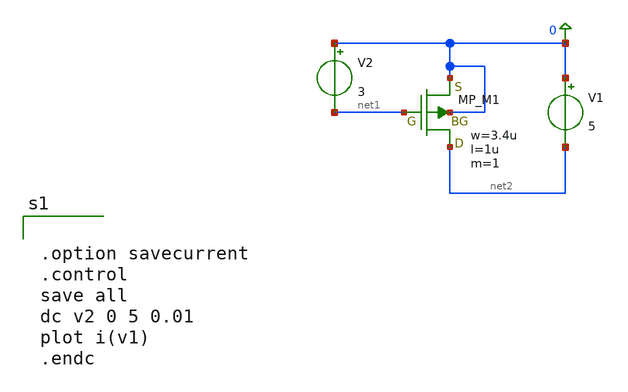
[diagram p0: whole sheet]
** sch_path: member_project/JJY_Receiver/Masahiro/jjy_recv/buffer/.sch
**.subckt .sch
XM1 net2 net1 0 0 PMOS w=3.4u l=1u as=0 ad=0 ps=0 pd=0 nrd=0 nrs=0 m=1
V1 0 net2 5
V2 0 net1 3
**** begin user architecture code
 .include $::LIB/ip62_models


.option savecurrent
.control
save all
dc v2 0 5 0.01
plot i(v1)
.endc


**** end user architecture code
**.ends
.end
